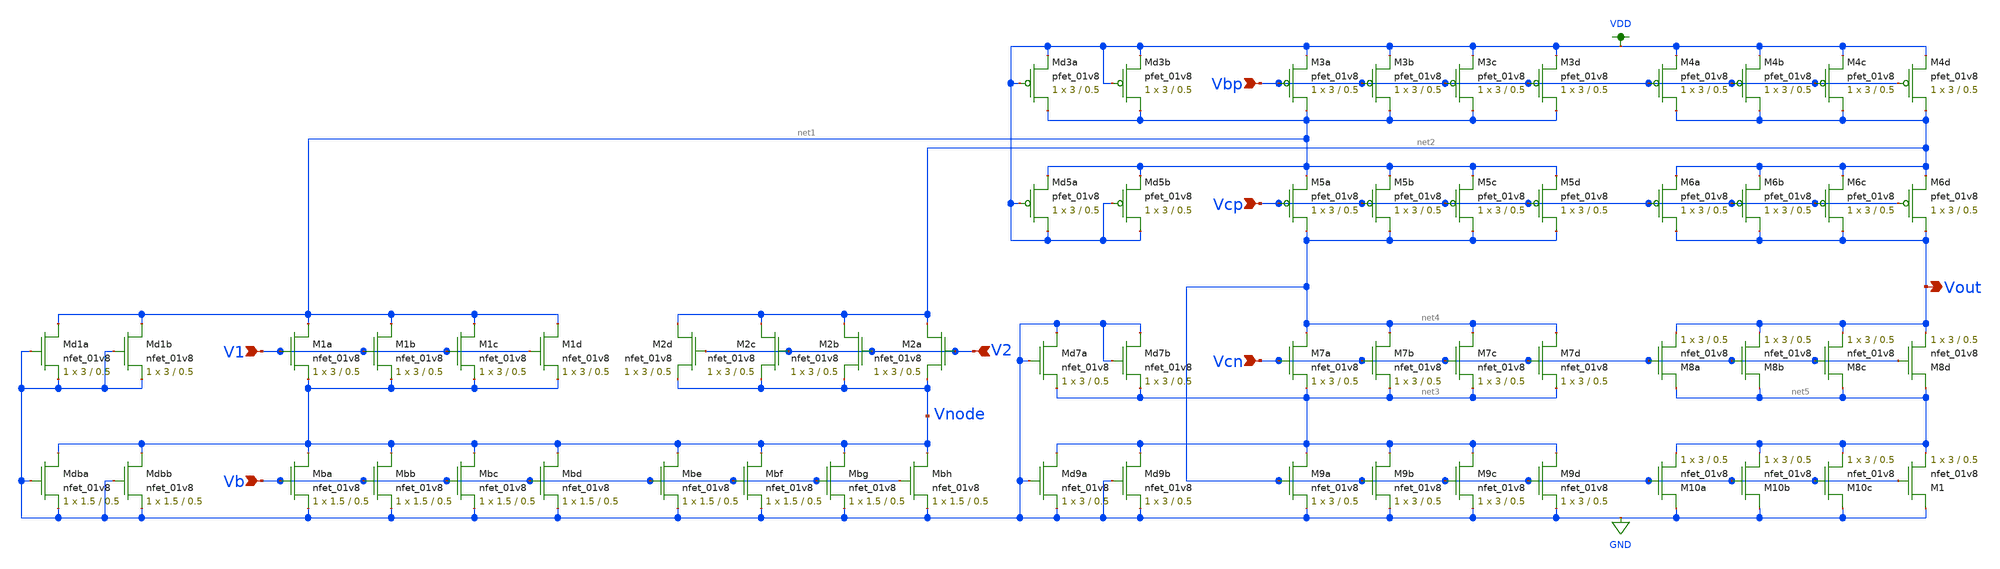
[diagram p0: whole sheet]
** sch_path: xschem/other_project_files/opamp_schematic_lvs.sch
**.subckt opamp_schematic_lvs Vbp Vcp Vcn V2 V1 Vb Vout
*.ipin Vbp
*.ipin Vcp
*.ipin Vcn
*.ipin V2
*.ipin V1
*.ipin Vb
*.opin Vout
XM1a net1 V1 Vnode GND sky130_fd_pr__nfet_01v8 L=0.5 W=3 nf=1 ad='int((nf+1)/2) * W/nf * 0.29' as='int((nf+2)/2) * W/nf * 0.29'
+ pd='2*int((nf+1)/2) * (W/nf + 0.29)' ps='2*int((nf+2)/2) * (W/nf + 0.29)' nrd='0.29 / W' nrs='0.29 / W'
+ sa=0 sb=0 sd=0 mult=1 m=1
XM1b net1 V1 Vnode GND sky130_fd_pr__nfet_01v8 L=0.5 W=3 nf=1 ad='int((nf+1)/2) * W/nf * 0.29' as='int((nf+2)/2) * W/nf * 0.29'
+ pd='2*int((nf+1)/2) * (W/nf + 0.29)' ps='2*int((nf+2)/2) * (W/nf + 0.29)' nrd='0.29 / W' nrs='0.29 / W'
+ sa=0 sb=0 sd=0 mult=1 m=1
XM1c net1 V1 Vnode GND sky130_fd_pr__nfet_01v8 L=0.5 W=3 nf=1 ad='int((nf+1)/2) * W/nf * 0.29' as='int((nf+2)/2) * W/nf * 0.29'
+ pd='2*int((nf+1)/2) * (W/nf + 0.29)' ps='2*int((nf+2)/2) * (W/nf + 0.29)' nrd='0.29 / W' nrs='0.29 / W'
+ sa=0 sb=0 sd=0 mult=1 m=1
XM1d net1 V1 Vnode GND sky130_fd_pr__nfet_01v8 L=0.5 W=3 nf=1 ad='int((nf+1)/2) * W/nf * 0.29' as='int((nf+2)/2) * W/nf * 0.29'
+ pd='2*int((nf+1)/2) * (W/nf + 0.29)' ps='2*int((nf+2)/2) * (W/nf + 0.29)' nrd='0.29 / W' nrs='0.29 / W'
+ sa=0 sb=0 sd=0 mult=1 m=1
XM2a net2 V2 Vnode GND sky130_fd_pr__nfet_01v8 L=0.5 W=3 nf=1 ad='int((nf+1)/2) * W/nf * 0.29' as='int((nf+2)/2) * W/nf * 0.29'
+ pd='2*int((nf+1)/2) * (W/nf + 0.29)' ps='2*int((nf+2)/2) * (W/nf + 0.29)' nrd='0.29 / W' nrs='0.29 / W'
+ sa=0 sb=0 sd=0 mult=1 m=1
XM2b net2 V2 Vnode GND sky130_fd_pr__nfet_01v8 L=0.5 W=3 nf=1 ad='int((nf+1)/2) * W/nf * 0.29' as='int((nf+2)/2) * W/nf * 0.29'
+ pd='2*int((nf+1)/2) * (W/nf + 0.29)' ps='2*int((nf+2)/2) * (W/nf + 0.29)' nrd='0.29 / W' nrs='0.29 / W'
+ sa=0 sb=0 sd=0 mult=1 m=1
XM2c net2 V2 Vnode GND sky130_fd_pr__nfet_01v8 L=0.5 W=3 nf=1 ad='int((nf+1)/2) * W/nf * 0.29' as='int((nf+2)/2) * W/nf * 0.29'
+ pd='2*int((nf+1)/2) * (W/nf + 0.29)' ps='2*int((nf+2)/2) * (W/nf + 0.29)' nrd='0.29 / W' nrs='0.29 / W'
+ sa=0 sb=0 sd=0 mult=1 m=1
XM2d net2 V2 Vnode GND sky130_fd_pr__nfet_01v8 L=0.5 W=3 nf=1 ad='int((nf+1)/2) * W/nf * 0.29' as='int((nf+2)/2) * W/nf * 0.29'
+ pd='2*int((nf+1)/2) * (W/nf + 0.29)' ps='2*int((nf+2)/2) * (W/nf + 0.29)' nrd='0.29 / W' nrs='0.29 / W'
+ sa=0 sb=0 sd=0 mult=1 m=1
XMba Vnode Vb GND GND sky130_fd_pr__nfet_01v8 L=0.5 W=1.5 nf=1 ad='int((nf+1)/2) * W/nf * 0.29' as='int((nf+2)/2) * W/nf * 0.29'
+ pd='2*int((nf+1)/2) * (W/nf + 0.29)' ps='2*int((nf+2)/2) * (W/nf + 0.29)' nrd='0.29 / W' nrs='0.29 / W'
+ sa=0 sb=0 sd=0 mult=1 m=1
XMbb Vnode Vb GND GND sky130_fd_pr__nfet_01v8 L=0.5 W=1.5 nf=1 ad='int((nf+1)/2) * W/nf * 0.29' as='int((nf+2)/2) * W/nf * 0.29'
+ pd='2*int((nf+1)/2) * (W/nf + 0.29)' ps='2*int((nf+2)/2) * (W/nf + 0.29)' nrd='0.29 / W' nrs='0.29 / W'
+ sa=0 sb=0 sd=0 mult=1 m=1
XMbc Vnode Vb GND GND sky130_fd_pr__nfet_01v8 L=0.5 W=1.5 nf=1 ad='int((nf+1)/2) * W/nf * 0.29' as='int((nf+2)/2) * W/nf * 0.29'
+ pd='2*int((nf+1)/2) * (W/nf + 0.29)' ps='2*int((nf+2)/2) * (W/nf + 0.29)' nrd='0.29 / W' nrs='0.29 / W'
+ sa=0 sb=0 sd=0 mult=1 m=1
XMbd Vnode Vb GND GND sky130_fd_pr__nfet_01v8 L=0.5 W=1.5 nf=1 ad='int((nf+1)/2) * W/nf * 0.29' as='int((nf+2)/2) * W/nf * 0.29'
+ pd='2*int((nf+1)/2) * (W/nf + 0.29)' ps='2*int((nf+2)/2) * (W/nf + 0.29)' nrd='0.29 / W' nrs='0.29 / W'
+ sa=0 sb=0 sd=0 mult=1 m=1
XMbe Vnode Vb GND GND sky130_fd_pr__nfet_01v8 L=0.5 W=1.5 nf=1 ad='int((nf+1)/2) * W/nf * 0.29' as='int((nf+2)/2) * W/nf * 0.29'
+ pd='2*int((nf+1)/2) * (W/nf + 0.29)' ps='2*int((nf+2)/2) * (W/nf + 0.29)' nrd='0.29 / W' nrs='0.29 / W'
+ sa=0 sb=0 sd=0 mult=1 m=1
XMbf Vnode Vb GND GND sky130_fd_pr__nfet_01v8 L=0.5 W=1.5 nf=1 ad='int((nf+1)/2) * W/nf * 0.29' as='int((nf+2)/2) * W/nf * 0.29'
+ pd='2*int((nf+1)/2) * (W/nf + 0.29)' ps='2*int((nf+2)/2) * (W/nf + 0.29)' nrd='0.29 / W' nrs='0.29 / W'
+ sa=0 sb=0 sd=0 mult=1 m=1
XMbg Vnode Vb GND GND sky130_fd_pr__nfet_01v8 L=0.5 W=1.5 nf=1 ad='int((nf+1)/2) * W/nf * 0.29' as='int((nf+2)/2) * W/nf * 0.29'
+ pd='2*int((nf+1)/2) * (W/nf + 0.29)' ps='2*int((nf+2)/2) * (W/nf + 0.29)' nrd='0.29 / W' nrs='0.29 / W'
+ sa=0 sb=0 sd=0 mult=1 m=1
XMbh Vnode Vb GND GND sky130_fd_pr__nfet_01v8 L=0.5 W=1.5 nf=1 ad='int((nf+1)/2) * W/nf * 0.29' as='int((nf+2)/2) * W/nf * 0.29'
+ pd='2*int((nf+1)/2) * (W/nf + 0.29)' ps='2*int((nf+2)/2) * (W/nf + 0.29)' nrd='0.29 / W' nrs='0.29 / W'
+ sa=0 sb=0 sd=0 mult=1 m=1
XM7a net4 Vcn net3 GND sky130_fd_pr__nfet_01v8 L=0.5 W=3 nf=1 ad='int((nf+1)/2) * W/nf * 0.29' as='int((nf+2)/2) * W/nf * 0.29'
+ pd='2*int((nf+1)/2) * (W/nf + 0.29)' ps='2*int((nf+2)/2) * (W/nf + 0.29)' nrd='0.29 / W' nrs='0.29 / W'
+ sa=0 sb=0 sd=0 mult=1 m=1
XM7b net4 Vcn net3 GND sky130_fd_pr__nfet_01v8 L=0.5 W=3 nf=1 ad='int((nf+1)/2) * W/nf * 0.29' as='int((nf+2)/2) * W/nf * 0.29'
+ pd='2*int((nf+1)/2) * (W/nf + 0.29)' ps='2*int((nf+2)/2) * (W/nf + 0.29)' nrd='0.29 / W' nrs='0.29 / W'
+ sa=0 sb=0 sd=0 mult=1 m=1
XM7c net4 Vcn net3 GND sky130_fd_pr__nfet_01v8 L=0.5 W=3 nf=1 ad='int((nf+1)/2) * W/nf * 0.29' as='int((nf+2)/2) * W/nf * 0.29'
+ pd='2*int((nf+1)/2) * (W/nf + 0.29)' ps='2*int((nf+2)/2) * (W/nf + 0.29)' nrd='0.29 / W' nrs='0.29 / W'
+ sa=0 sb=0 sd=0 mult=1 m=1
XM7d net4 Vcn net3 GND sky130_fd_pr__nfet_01v8 L=0.5 W=3 nf=1 ad='int((nf+1)/2) * W/nf * 0.29' as='int((nf+2)/2) * W/nf * 0.29'
+ pd='2*int((nf+1)/2) * (W/nf + 0.29)' ps='2*int((nf+2)/2) * (W/nf + 0.29)' nrd='0.29 / W' nrs='0.29 / W'
+ sa=0 sb=0 sd=0 mult=1 m=1
XM8a net5 Vcn Vout GND sky130_fd_pr__nfet_01v8 L=0.5 W=3 nf=1 ad='int((nf+1)/2) * W/nf * 0.29' as='int((nf+2)/2) * W/nf * 0.29'
+ pd='2*int((nf+1)/2) * (W/nf + 0.29)' ps='2*int((nf+2)/2) * (W/nf + 0.29)' nrd='0.29 / W' nrs='0.29 / W'
+ sa=0 sb=0 sd=0 mult=1 m=1
XM8b net5 Vcn Vout GND sky130_fd_pr__nfet_01v8 L=0.5 W=3 nf=1 ad='int((nf+1)/2) * W/nf * 0.29' as='int((nf+2)/2) * W/nf * 0.29'
+ pd='2*int((nf+1)/2) * (W/nf + 0.29)' ps='2*int((nf+2)/2) * (W/nf + 0.29)' nrd='0.29 / W' nrs='0.29 / W'
+ sa=0 sb=0 sd=0 mult=1 m=1
XM8c net5 Vcn Vout GND sky130_fd_pr__nfet_01v8 L=0.5 W=3 nf=1 ad='int((nf+1)/2) * W/nf * 0.29' as='int((nf+2)/2) * W/nf * 0.29'
+ pd='2*int((nf+1)/2) * (W/nf + 0.29)' ps='2*int((nf+2)/2) * (W/nf + 0.29)' nrd='0.29 / W' nrs='0.29 / W'
+ sa=0 sb=0 sd=0 mult=1 m=1
XM8d net5 Vcn Vout GND sky130_fd_pr__nfet_01v8 L=0.5 W=3 nf=1 ad='int((nf+1)/2) * W/nf * 0.29' as='int((nf+2)/2) * W/nf * 0.29'
+ pd='2*int((nf+1)/2) * (W/nf + 0.29)' ps='2*int((nf+2)/2) * (W/nf + 0.29)' nrd='0.29 / W' nrs='0.29 / W'
+ sa=0 sb=0 sd=0 mult=1 m=1
XM9a net3 net4 GND GND sky130_fd_pr__nfet_01v8 L=0.5 W=3 nf=1 ad='int((nf+1)/2) * W/nf * 0.29' as='int((nf+2)/2) * W/nf * 0.29'
+ pd='2*int((nf+1)/2) * (W/nf + 0.29)' ps='2*int((nf+2)/2) * (W/nf + 0.29)' nrd='0.29 / W' nrs='0.29 / W'
+ sa=0 sb=0 sd=0 mult=1 m=1
XM9b net3 net4 GND GND sky130_fd_pr__nfet_01v8 L=0.5 W=3 nf=1 ad='int((nf+1)/2) * W/nf * 0.29' as='int((nf+2)/2) * W/nf * 0.29'
+ pd='2*int((nf+1)/2) * (W/nf + 0.29)' ps='2*int((nf+2)/2) * (W/nf + 0.29)' nrd='0.29 / W' nrs='0.29 / W'
+ sa=0 sb=0 sd=0 mult=1 m=1
XM9c net3 net4 GND GND sky130_fd_pr__nfet_01v8 L=0.5 W=3 nf=1 ad='int((nf+1)/2) * W/nf * 0.29' as='int((nf+2)/2) * W/nf * 0.29'
+ pd='2*int((nf+1)/2) * (W/nf + 0.29)' ps='2*int((nf+2)/2) * (W/nf + 0.29)' nrd='0.29 / W' nrs='0.29 / W'
+ sa=0 sb=0 sd=0 mult=1 m=1
XM9d net3 net4 GND GND sky130_fd_pr__nfet_01v8 L=0.5 W=3 nf=1 ad='int((nf+1)/2) * W/nf * 0.29' as='int((nf+2)/2) * W/nf * 0.29'
+ pd='2*int((nf+1)/2) * (W/nf + 0.29)' ps='2*int((nf+2)/2) * (W/nf + 0.29)' nrd='0.29 / W' nrs='0.29 / W'
+ sa=0 sb=0 sd=0 mult=1 m=1
XM10a GND net4 net5 GND sky130_fd_pr__nfet_01v8 L=0.5 W=3 nf=1 ad='int((nf+1)/2) * W/nf * 0.29' as='int((nf+2)/2) * W/nf * 0.29'
+ pd='2*int((nf+1)/2) * (W/nf + 0.29)' ps='2*int((nf+2)/2) * (W/nf + 0.29)' nrd='0.29 / W' nrs='0.29 / W'
+ sa=0 sb=0 sd=0 mult=1 m=1
XM10b GND net4 net5 GND sky130_fd_pr__nfet_01v8 L=0.5 W=3 nf=1 ad='int((nf+1)/2) * W/nf * 0.29' as='int((nf+2)/2) * W/nf * 0.29'
+ pd='2*int((nf+1)/2) * (W/nf + 0.29)' ps='2*int((nf+2)/2) * (W/nf + 0.29)' nrd='0.29 / W' nrs='0.29 / W'
+ sa=0 sb=0 sd=0 mult=1 m=1
XM10c GND net4 net5 GND sky130_fd_pr__nfet_01v8 L=0.5 W=3 nf=1 ad='int((nf+1)/2) * W/nf * 0.29' as='int((nf+2)/2) * W/nf * 0.29'
+ pd='2*int((nf+1)/2) * (W/nf + 0.29)' ps='2*int((nf+2)/2) * (W/nf + 0.29)' nrd='0.29 / W' nrs='0.29 / W'
+ sa=0 sb=0 sd=0 mult=1 m=1
XM1 GND net4 net5 GND sky130_fd_pr__nfet_01v8 L=0.5 W=3 nf=1 ad='int((nf+1)/2) * W/nf * 0.29' as='int((nf+2)/2) * W/nf * 0.29'
+ pd='2*int((nf+1)/2) * (W/nf + 0.29)' ps='2*int((nf+2)/2) * (W/nf + 0.29)' nrd='0.29 / W' nrs='0.29 / W'
+ sa=0 sb=0 sd=0 mult=1 m=1
XM5a net4 Vcp net1 VDD sky130_fd_pr__pfet_01v8 L=0.5 W=3 nf=1 ad='int((nf+1)/2) * W/nf * 0.29' as='int((nf+2)/2) * W/nf * 0.29'
+ pd='2*int((nf+1)/2) * (W/nf + 0.29)' ps='2*int((nf+2)/2) * (W/nf + 0.29)' nrd='0.29 / W' nrs='0.29 / W'
+ sa=0 sb=0 sd=0 mult=1 m=1
XM5b net4 Vcp net1 VDD sky130_fd_pr__pfet_01v8 L=0.5 W=3 nf=1 ad='int((nf+1)/2) * W/nf * 0.29' as='int((nf+2)/2) * W/nf * 0.29'
+ pd='2*int((nf+1)/2) * (W/nf + 0.29)' ps='2*int((nf+2)/2) * (W/nf + 0.29)' nrd='0.29 / W' nrs='0.29 / W'
+ sa=0 sb=0 sd=0 mult=1 m=1
XM5c net4 Vcp net1 VDD sky130_fd_pr__pfet_01v8 L=0.5 W=3 nf=1 ad='int((nf+1)/2) * W/nf * 0.29' as='int((nf+2)/2) * W/nf * 0.29'
+ pd='2*int((nf+1)/2) * (W/nf + 0.29)' ps='2*int((nf+2)/2) * (W/nf + 0.29)' nrd='0.29 / W' nrs='0.29 / W'
+ sa=0 sb=0 sd=0 mult=1 m=1
XM5d net4 Vcp net1 VDD sky130_fd_pr__pfet_01v8 L=0.5 W=3 nf=1 ad='int((nf+1)/2) * W/nf * 0.29' as='int((nf+2)/2) * W/nf * 0.29'
+ pd='2*int((nf+1)/2) * (W/nf + 0.29)' ps='2*int((nf+2)/2) * (W/nf + 0.29)' nrd='0.29 / W' nrs='0.29 / W'
+ sa=0 sb=0 sd=0 mult=1 m=1
XM6a Vout Vcp net2 VDD sky130_fd_pr__pfet_01v8 L=0.5 W=3 nf=1 ad='int((nf+1)/2) * W/nf * 0.29' as='int((nf+2)/2) * W/nf * 0.29'
+ pd='2*int((nf+1)/2) * (W/nf + 0.29)' ps='2*int((nf+2)/2) * (W/nf + 0.29)' nrd='0.29 / W' nrs='0.29 / W'
+ sa=0 sb=0 sd=0 mult=1 m=1
XM6b Vout Vcp net2 VDD sky130_fd_pr__pfet_01v8 L=0.5 W=3 nf=1 ad='int((nf+1)/2) * W/nf * 0.29' as='int((nf+2)/2) * W/nf * 0.29'
+ pd='2*int((nf+1)/2) * (W/nf + 0.29)' ps='2*int((nf+2)/2) * (W/nf + 0.29)' nrd='0.29 / W' nrs='0.29 / W'
+ sa=0 sb=0 sd=0 mult=1 m=1
XM6c Vout Vcp net2 VDD sky130_fd_pr__pfet_01v8 L=0.5 W=3 nf=1 ad='int((nf+1)/2) * W/nf * 0.29' as='int((nf+2)/2) * W/nf * 0.29'
+ pd='2*int((nf+1)/2) * (W/nf + 0.29)' ps='2*int((nf+2)/2) * (W/nf + 0.29)' nrd='0.29 / W' nrs='0.29 / W'
+ sa=0 sb=0 sd=0 mult=1 m=1
XM6d Vout Vcp net2 VDD sky130_fd_pr__pfet_01v8 L=0.5 W=3 nf=1 ad='int((nf+1)/2) * W/nf * 0.29' as='int((nf+2)/2) * W/nf * 0.29'
+ pd='2*int((nf+1)/2) * (W/nf + 0.29)' ps='2*int((nf+2)/2) * (W/nf + 0.29)' nrd='0.29 / W' nrs='0.29 / W'
+ sa=0 sb=0 sd=0 mult=1 m=1
XM3a net1 Vbp VDD VDD sky130_fd_pr__pfet_01v8 L=0.5 W=3 nf=1 ad='int((nf+1)/2) * W/nf * 0.29' as='int((nf+2)/2) * W/nf * 0.29'
+ pd='2*int((nf+1)/2) * (W/nf + 0.29)' ps='2*int((nf+2)/2) * (W/nf + 0.29)' nrd='0.29 / W' nrs='0.29 / W'
+ sa=0 sb=0 sd=0 mult=1 m=1
XM3b net1 Vbp VDD VDD sky130_fd_pr__pfet_01v8 L=0.5 W=3 nf=1 ad='int((nf+1)/2) * W/nf * 0.29' as='int((nf+2)/2) * W/nf * 0.29'
+ pd='2*int((nf+1)/2) * (W/nf + 0.29)' ps='2*int((nf+2)/2) * (W/nf + 0.29)' nrd='0.29 / W' nrs='0.29 / W'
+ sa=0 sb=0 sd=0 mult=1 m=1
XM3c net1 Vbp VDD VDD sky130_fd_pr__pfet_01v8 L=0.5 W=3 nf=1 ad='int((nf+1)/2) * W/nf * 0.29' as='int((nf+2)/2) * W/nf * 0.29'
+ pd='2*int((nf+1)/2) * (W/nf + 0.29)' ps='2*int((nf+2)/2) * (W/nf + 0.29)' nrd='0.29 / W' nrs='0.29 / W'
+ sa=0 sb=0 sd=0 mult=1 m=1
XM3d net1 Vbp VDD VDD sky130_fd_pr__pfet_01v8 L=0.5 W=3 nf=1 ad='int((nf+1)/2) * W/nf * 0.29' as='int((nf+2)/2) * W/nf * 0.29'
+ pd='2*int((nf+1)/2) * (W/nf + 0.29)' ps='2*int((nf+2)/2) * (W/nf + 0.29)' nrd='0.29 / W' nrs='0.29 / W'
+ sa=0 sb=0 sd=0 mult=1 m=1
XM4a net2 Vbp VDD VDD sky130_fd_pr__pfet_01v8 L=0.5 W=3 nf=1 ad='int((nf+1)/2) * W/nf * 0.29' as='int((nf+2)/2) * W/nf * 0.29'
+ pd='2*int((nf+1)/2) * (W/nf + 0.29)' ps='2*int((nf+2)/2) * (W/nf + 0.29)' nrd='0.29 / W' nrs='0.29 / W'
+ sa=0 sb=0 sd=0 mult=1 m=1
XM4b net2 Vbp VDD VDD sky130_fd_pr__pfet_01v8 L=0.5 W=3 nf=1 ad='int((nf+1)/2) * W/nf * 0.29' as='int((nf+2)/2) * W/nf * 0.29'
+ pd='2*int((nf+1)/2) * (W/nf + 0.29)' ps='2*int((nf+2)/2) * (W/nf + 0.29)' nrd='0.29 / W' nrs='0.29 / W'
+ sa=0 sb=0 sd=0 mult=1 m=1
XM4c net2 Vbp VDD VDD sky130_fd_pr__pfet_01v8 L=0.5 W=3 nf=1 ad='int((nf+1)/2) * W/nf * 0.29' as='int((nf+2)/2) * W/nf * 0.29'
+ pd='2*int((nf+1)/2) * (W/nf + 0.29)' ps='2*int((nf+2)/2) * (W/nf + 0.29)' nrd='0.29 / W' nrs='0.29 / W'
+ sa=0 sb=0 sd=0 mult=1 m=1
XM4d net2 Vbp VDD VDD sky130_fd_pr__pfet_01v8 L=0.5 W=3 nf=1 ad='int((nf+1)/2) * W/nf * 0.29' as='int((nf+2)/2) * W/nf * 0.29'
+ pd='2*int((nf+1)/2) * (W/nf + 0.29)' ps='2*int((nf+2)/2) * (W/nf + 0.29)' nrd='0.29 / W' nrs='0.29 / W'
+ sa=0 sb=0 sd=0 mult=1 m=1
XMd3b net1 VDD VDD VDD sky130_fd_pr__pfet_01v8 L=0.5 W=3 nf=1 ad='int((nf+1)/2) * W/nf * 0.29' as='int((nf+2)/2) * W/nf * 0.29'
+ pd='2*int((nf+1)/2) * (W/nf + 0.29)' ps='2*int((nf+2)/2) * (W/nf + 0.29)' nrd='0.29 / W' nrs='0.29 / W'
+ sa=0 sb=0 sd=0 mult=1 m=1
XMd3a net1 VDD VDD VDD sky130_fd_pr__pfet_01v8 L=0.5 W=3 nf=1 ad='int((nf+1)/2) * W/nf * 0.29' as='int((nf+2)/2) * W/nf * 0.29'
+ pd='2*int((nf+1)/2) * (W/nf + 0.29)' ps='2*int((nf+2)/2) * (W/nf + 0.29)' nrd='0.29 / W' nrs='0.29 / W'
+ sa=0 sb=0 sd=0 mult=1 m=1
XMd5b VDD VDD net1 VDD sky130_fd_pr__pfet_01v8 L=0.5 W=3 nf=1 ad='int((nf+1)/2) * W/nf * 0.29' as='int((nf+2)/2) * W/nf * 0.29'
+ pd='2*int((nf+1)/2) * (W/nf + 0.29)' ps='2*int((nf+2)/2) * (W/nf + 0.29)' nrd='0.29 / W' nrs='0.29 / W'
+ sa=0 sb=0 sd=0 mult=1 m=1
XMd5a VDD VDD net1 VDD sky130_fd_pr__pfet_01v8 L=0.5 W=3 nf=1 ad='int((nf+1)/2) * W/nf * 0.29' as='int((nf+2)/2) * W/nf * 0.29'
+ pd='2*int((nf+1)/2) * (W/nf + 0.29)' ps='2*int((nf+2)/2) * (W/nf + 0.29)' nrd='0.29 / W' nrs='0.29 / W'
+ sa=0 sb=0 sd=0 mult=1 m=1
XMd7a GND GND net3 GND sky130_fd_pr__nfet_01v8 L=0.5 W=3 nf=1 ad='int((nf+1)/2) * W/nf * 0.29' as='int((nf+2)/2) * W/nf * 0.29'
+ pd='2*int((nf+1)/2) * (W/nf + 0.29)' ps='2*int((nf+2)/2) * (W/nf + 0.29)' nrd='0.29 / W' nrs='0.29 / W'
+ sa=0 sb=0 sd=0 mult=1 m=1
XMd7b GND GND net3 GND sky130_fd_pr__nfet_01v8 L=0.5 W=3 nf=1 ad='int((nf+1)/2) * W/nf * 0.29' as='int((nf+2)/2) * W/nf * 0.29'
+ pd='2*int((nf+1)/2) * (W/nf + 0.29)' ps='2*int((nf+2)/2) * (W/nf + 0.29)' nrd='0.29 / W' nrs='0.29 / W'
+ sa=0 sb=0 sd=0 mult=1 m=1
XMd9a net3 GND GND GND sky130_fd_pr__nfet_01v8 L=0.5 W=3 nf=1 ad='int((nf+1)/2) * W/nf * 0.29' as='int((nf+2)/2) * W/nf * 0.29'
+ pd='2*int((nf+1)/2) * (W/nf + 0.29)' ps='2*int((nf+2)/2) * (W/nf + 0.29)' nrd='0.29 / W' nrs='0.29 / W'
+ sa=0 sb=0 sd=0 mult=1 m=1
XMd9b net3 GND GND GND sky130_fd_pr__nfet_01v8 L=0.5 W=3 nf=1 ad='int((nf+1)/2) * W/nf * 0.29' as='int((nf+2)/2) * W/nf * 0.29'
+ pd='2*int((nf+1)/2) * (W/nf + 0.29)' ps='2*int((nf+2)/2) * (W/nf + 0.29)' nrd='0.29 / W' nrs='0.29 / W'
+ sa=0 sb=0 sd=0 mult=1 m=1
XMd1a net1 GND GND GND sky130_fd_pr__nfet_01v8 L=0.5 W=3 nf=1 ad='int((nf+1)/2) * W/nf * 0.29' as='int((nf+2)/2) * W/nf * 0.29'
+ pd='2*int((nf+1)/2) * (W/nf + 0.29)' ps='2*int((nf+2)/2) * (W/nf + 0.29)' nrd='0.29 / W' nrs='0.29 / W'
+ sa=0 sb=0 sd=0 mult=1 m=1
XMd1b net1 GND GND GND sky130_fd_pr__nfet_01v8 L=0.5 W=3 nf=1 ad='int((nf+1)/2) * W/nf * 0.29' as='int((nf+2)/2) * W/nf * 0.29'
+ pd='2*int((nf+1)/2) * (W/nf + 0.29)' ps='2*int((nf+2)/2) * (W/nf + 0.29)' nrd='0.29 / W' nrs='0.29 / W'
+ sa=0 sb=0 sd=0 mult=1 m=1
XMdba Vnode GND GND GND sky130_fd_pr__nfet_01v8 L=0.5 W=1.5 nf=1 ad='int((nf+1)/2) * W/nf * 0.29' as='int((nf+2)/2) * W/nf * 0.29'
+ pd='2*int((nf+1)/2) * (W/nf + 0.29)' ps='2*int((nf+2)/2) * (W/nf + 0.29)' nrd='0.29 / W' nrs='0.29 / W'
+ sa=0 sb=0 sd=0 mult=1 m=1
XMdbb Vnode GND GND GND sky130_fd_pr__nfet_01v8 L=0.5 W=1.5 nf=1 ad='int((nf+1)/2) * W/nf * 0.29' as='int((nf+2)/2) * W/nf * 0.29'
+ pd='2*int((nf+1)/2) * (W/nf + 0.29)' ps='2*int((nf+2)/2) * (W/nf + 0.29)' nrd='0.29 / W' nrs='0.29 / W'
+ sa=0 sb=0 sd=0 mult=1 m=1
**.ends
.GLOBAL VDD
.GLOBAL GND
.end
